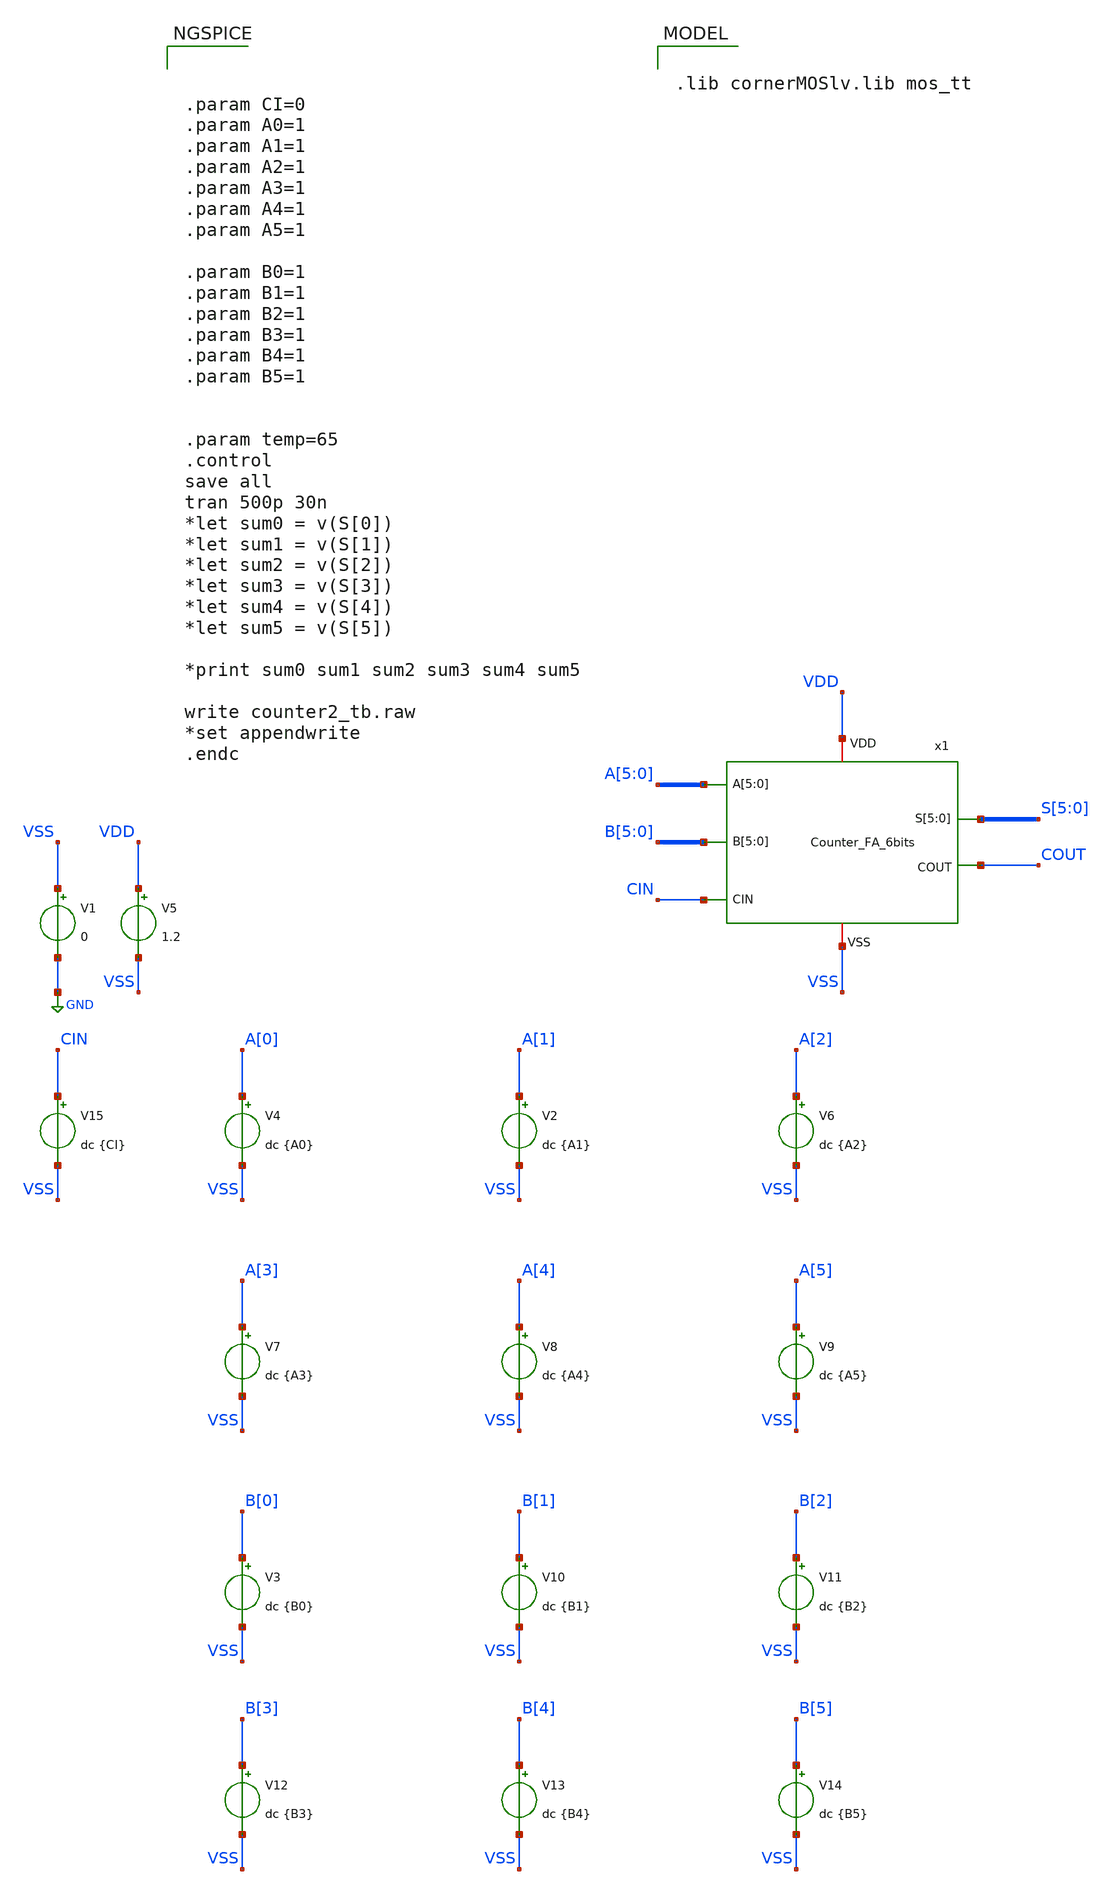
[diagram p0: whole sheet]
** sch_path: ADC8711-main/testbenches/tran/xschem/tb_Counter_FA_6bits.sch
**.subckt tb_Counter_FA_6bits
V1 VSS GND 0
V3 B[0] VSS dc {B0}
V5 VDD VSS 1.2
V4 A[0] VSS dc {A0}
x1 S[5] S[4] S[3] S[2] S[1] S[0] A[5] A[4] A[3] A[2] A[1] A[0] VDD COUT B[5] B[4] B[3] B[2] B[1]
+ B[0] VSS CIN Counter_FA_6bits
V2 A[1] VSS dc {A1}
V6 A[2] VSS dc {A2}
V7 A[3] VSS dc {A3}
V8 A[4] VSS dc {A4}
V9 A[5] VSS dc {A5}
V10 B[1] VSS dc {B1}
V11 B[2] VSS dc {B2}
V12 B[3] VSS dc {B3}
V13 B[4] VSS dc {B4}
V14 B[5] VSS dc {B5}
V15 CIN VSS dc {CI}
**** begin user architecture code



.param CI=0
.param A0=1
.param A1=1
.param A2=1
.param A3=1
.param A4=1
.param A5=1

.param B0=1
.param B1=1
.param B2=1
.param B3=1
.param B4=1
.param B5=1


.param temp=65
.control
save all
tran 500p 30n
*let sum0 = v(S[0])
*let sum1 = v(S[1])
*let sum2 = v(S[2])
*let sum3 = v(S[3])
*let sum4 = v(S[4])
*let sum5 = v(S[5])

*print sum0 sum1 sum2 sum3 sum4 sum5

write counter2_tb.raw
*set appendwrite
.endc




.lib cornerMOSlv.lib mos_tt

**** end user architecture code
**.ends
.GLOBAL GND
.end
